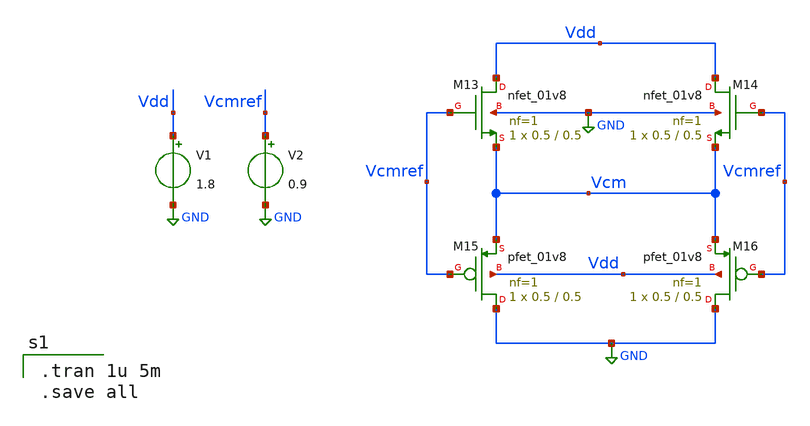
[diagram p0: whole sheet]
** sch_path: xschem/xschemfiles/test.sch
**.subckt test
XM13 Vdd Vcmref Vcm GND sky130_fd_pr__nfet_01v8 L=0.5 W=0.5 nf=1 ad='int((nf+1)/2) * W/nf * 0.29' as='int((nf+2)/2) * W/nf * 0.29'
+ pd='2*int((nf+1)/2) * (W/nf + 0.29)' ps='2*int((nf+2)/2) * (W/nf + 0.29)' nrd='0.29 / W' nrs='0.29 / W'
+ sa=0 sb=0 sd=0 mult=1 m=1
XM14 Vdd Vcmref Vcm GND sky130_fd_pr__nfet_01v8 L=0.5 W=0.5 nf=1 ad='int((nf+1)/2) * W/nf * 0.29' as='int((nf+2)/2) * W/nf * 0.29'
+ pd='2*int((nf+1)/2) * (W/nf + 0.29)' ps='2*int((nf+2)/2) * (W/nf + 0.29)' nrd='0.29 / W' nrs='0.29 / W'
+ sa=0 sb=0 sd=0 mult=1 m=1
XM15 GND Vcmref Vcm Vdd sky130_fd_pr__pfet_01v8 L=0.5 W=0.5 nf=1 ad='int((nf+1)/2) * W/nf * 0.29' as='int((nf+2)/2) * W/nf * 0.29'
+ pd='2*int((nf+1)/2) * (W/nf + 0.29)' ps='2*int((nf+2)/2) * (W/nf + 0.29)' nrd='0.29 / W' nrs='0.29 / W'
+ sa=0 sb=0 sd=0 mult=1 m=1
XM16 GND Vcmref Vcm Vdd sky130_fd_pr__pfet_01v8 L=0.5 W=0.5 nf=1 ad='int((nf+1)/2) * W/nf * 0.29' as='int((nf+2)/2) * W/nf * 0.29'
+ pd='2*int((nf+1)/2) * (W/nf + 0.29)' ps='2*int((nf+2)/2) * (W/nf + 0.29)' nrd='0.29 / W' nrs='0.29 / W'
+ sa=0 sb=0 sd=0 mult=1 m=1
V1 Vdd GND 1.8
V2 Vcmref GND 0.9
**** begin user architecture code

** opencircuitdesign pdks install
.lib $::SKYWATER_MODELS/sky130.lib.spice tt



.tran 1u 5m
.save all

**** end user architecture code
**.ends
.GLOBAL GND
.end
